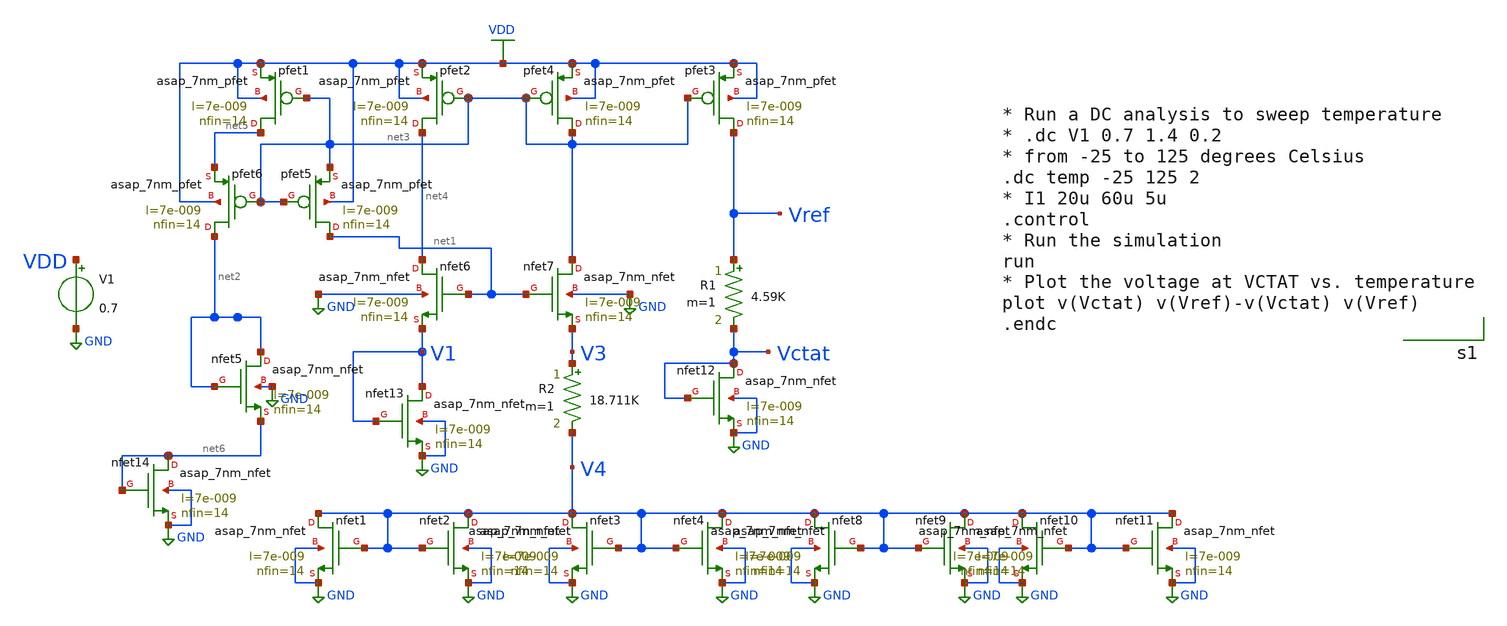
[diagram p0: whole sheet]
** sch_path: xschem/Circuits/BGR_Current_mirror.sch
* AsahiroKenpachi/asap_7nm_Xschem/asap_7nm_nfet.sym:
* Copyright 2021 Stefan Frederik Schippers
* Licensed under the Apache License, Version 2.0 (the "License");
**.subckt BGR_Current_mirror
Xnfet5 net2 net2 net6 GND asap_7nm_nfet l=7e-009 nfin=14
Xpfet1 net5 net3 VDD VDD asap_7nm_pfet l=7e-009 nfin=14
Xpfet2 net4 net3 VDD VDD asap_7nm_pfet l=7e-009 nfin=14
Xpfet3 Vref net3 VDD VDD asap_7nm_pfet l=7e-009 nfin=14
Xpfet4 net3 net3 VDD VDD asap_7nm_pfet l=7e-009 nfin=14
Xpfet5 net1 net3 net3 VDD asap_7nm_pfet l=7e-009 nfin=14
Xnfet1 V4 V4 GND GND asap_7nm_nfet l=7e-009 nfin=14
Xnfet2 V4 V4 GND GND asap_7nm_nfet l=7e-009 nfin=14
Xnfet3 V4 V4 GND GND asap_7nm_nfet l=7e-009 nfin=14
Xnfet4 V4 V4 GND GND asap_7nm_nfet l=7e-009 nfin=14
Xnfet8 V4 V4 GND GND asap_7nm_nfet l=7e-009 nfin=14
Xnfet9 V4 V4 GND GND asap_7nm_nfet l=7e-009 nfin=14
Xnfet10 V4 V4 GND GND asap_7nm_nfet l=7e-009 nfin=14
Xnfet11 V4 V4 GND GND asap_7nm_nfet l=7e-009 nfin=14
Xnfet12 Vctat Vctat GND GND asap_7nm_nfet l=7e-009 nfin=14
V1 VDD GND 0.7
Xnfet13 V1 V1 GND GND asap_7nm_nfet l=7e-009 nfin=14
Xpfet6 net2 net3 net5 VDD asap_7nm_pfet l=7e-009 nfin=14
Xnfet14 net6 net6 GND GND asap_7nm_nfet l=7e-009 nfin=14
R2 V3 V4 18.711K m=1
R1 Vref Vctat 4.59K m=1
Xnfet6 net4 net1 V1 GND asap_7nm_nfet l=7e-009 nfin=14
Xnfet7 net3 net1 V3 GND asap_7nm_nfet l=7e-009 nfin=14
**** begin user architecture code


* Run a DC analysis to sweep temperature
* .dc V1 0.7 1.4 0.2
* from -25 to 125 degrees Celsius
.dc temp -25 125 2
* I1 20u 60u 5u
.control
* Run the simulation
run
* Plot the voltage at VCTAT vs. temperature
plot v(Vctat) v(Vref)-v(Vctat) v(Vref)
.endc


**** end user architecture code
**.ends
.GLOBAL GND
.GLOBAL VDD
**** begin user architecture code

.subckt asap_7nm_nfet S G D B l=@l nfin=@nfin
	nnmos_finfet S G D B BSIMCMG_osdi_N l=@l nfin=@nfin
.ends asap_7nm_nfet

.model BSIMCMG_osdi_N BSIMCMG_va (  TYPE = 1
************************************************************
*                         general                          *
************************************************************ version = 107             bulkmod = 1
*+               igcmod  = 1               igbmod  = 0              gidlmod = 1               iimod   = 0
*+               geomod  = 1               rdsmod  = 0              rgatemod= 0               rgeomod = 0
*+               shmod   = 0               nqsmod  = 0              coremod = 0               cgeomod = 0
*+               capmod  = 0               tnom    = 25             eot     = 1e-009          eotbox  = 1.4e-007
*+        eotacc  = 1e-010          tfin    = 6.5e-009       toxp    = 2.1e-009        nbody   = 1e+022
*+          phig    = 4.2466          epsrox  = 3.9            epsrsub = 11.9            easub   = 4.05
*+            ni0sub  = 1.1e+016        bg0sub  = 1.17           nc0sub  = 2.86e+025       nsd     = 2e+026
*+          ngate   = 0               nseg    = 5              l       = 2.1e-008        xl      = 1e-009
*+          lint    = -2e-009         dlc     = 0              dlbin   = 0               hfin    = 3.2e-008
*+        deltaw  = 0               deltawcv= 0              sdterm  = 0               epsrsp  = 3.9
*+             nfin    = 1 toxg    = 1.80e-009
************************************************************
*                            dc                            *
************************************************************ cit     = 0               cdsc    =
*+ 0.01            cdscd   = 0.01            dvt0    = 0.05           dvt1    = 0.47            phin    =
*+ 0.05            eta0    = 0.07            dsub    = 0.35           k1rsce  = 0               lpe0    = 0
*+               dvtshift= 0               qmfactor= 2.5            etaqm   = 0.54            qm0     = 0.001           pqm
*+     = 0.66            u0      = 0.0303         etamob  = 2               up      = 0               ua
*+      = 0.55            eu      = 1.2            ud      = 0               ucs     = 1
*+               rdswmin = 0               rdsw    = 200            wr      = 1               rswmin  = 0
*+               rdwmin  = 0               rshs    = 0              rshd    = 0               vsat    = 70000
*+           deltavsat= 0.2             ksativ  = 2              mexp    = 4               ptwg    = 30              pclm
*+    = 0.05            pclmg   = 0              pdibl1  = 0               pdibl2  = 0.002           drout
*+   = 1               pvag    = 0              fpitch  = 2.7e-008        rth0    = 0.225           cth0
*+    = 1.243e-006      wth0    = 2.6e-007       lcdscd  = 5e-005          lcdscdr = 5e-005          lrdsw
*+   = 0.2             lvsat   = 0
************************************************************
*                         leakage                          *
************************************************************ aigc    = 0.014           bigc    =
*+ 0.005           cigc    = 0.25            dlcigs  = 1e-009         dlcigd  = 1e-009          aigs    =
*+ 0.0115          aigd    = 0.0115          bigs    = 0.00332        bigd    = 0.00332         cigs    =
*+ 0.35            cigd    = 0.35            poxedge = 1.1            agidl   = 1e-012          agisl   =
*+ 1e-012          bgidl   = 10000000        bgisl   = 10000000       egidl   = 0.35            egisl   =
*+ 0.35
************************************************************
*                            rf                            *
************************************************************
************************************************************
*                         junction                         *
************************************************************
************************************************************
*                       capacitance                        *
************************************************************ cfs     = 0               cfd     = 0
*+               cgso    = 1.6e-010        cgdo    = 1.6e-010       cgsl    = 0               cgdl    = 0
*+               ckappas = 0.6             ckappad = 0.6            cgbo    = 0               cgbl    = 0
************************************************************
*                       temperature                        *
************************************************************ tbgasub = 0.000473        tbgbsub = 636
*+             kt1     = 0               kt1l    = 0              ute     = -0.7            utl     = 0
*+               ua1     = 0.001032        ud1     = 0              ucste   = -0.004775       at      = 0.001
*+           ptwgt   = 0.004           tmexp   = 0              prt     = 0               tgidl   = -0.007
*+          igt     = 2.5
************************************************************
*                          noise                           *
************************************************************
**)
.control
pre_osdi /home/hprcse/Documents/test/bsimcmg.osdi
.endc



.subckt asap_7nm_pfet S G D B l=@l nfin=@nfin
	npmos_finfet S G D B BSIMCMG_osdi_P l=@l nfin=@nfin
.ends asap_7nm_pfet

.model BSIMCMG_osdi_P BSIMCMG_va (  TYPE = 0

************************************************************
*                         general                          *
************************************************************ version = 107             bulkmod = 1
*+               igcmod  = 1               igbmod  = 0              gidlmod = 1               iimod   = 0
*+               geomod  = 1               rdsmod  = 0              rgatemod= 0               rgeomod = 0
*+               shmod   = 0               nqsmod  = 0              coremod = 0               cgeomod = 0
*+               capmod  = 0               tnom    = 25             eot     = 1e-009          eotbox  = 1.4e-007
*+        eotacc  = 3e-010          tfin    = 6.5e-009       toxp    = 2.1e-009        nbody   = 1e+022
*+          phig    = 4.9278          epsrox  = 3.9            epsrsub = 11.9            easub   = 4.05
*+            ni0sub  = 1.1e+016        bg0sub  = 1.17           nc0sub  = 2.86e+025       nsd     = 2e+026
*+          ngate   = 0               nseg    = 5              l       = 2.1e-008        xl      = 1e-009
*+          lint    = -2.5e-009       dlc     = 0              dlbin   = 0               hfin    = 3.2e-008
*+        deltaw  = 0               deltawcv= 0              sdterm  = 0               epsrsp  = 3.9
*+             nfin    = 1 toxg    = 1.8e-009
************************************************************
*                            dc                            *
************************************************************ cit     = 0               cdsc    =
*+ 0.003469        cdscd   = 0.001486        dvt0    = 0.05           dvt1    = 0.36            phin    = 0.05
*+            eta0    = 0.094           dsub    = 0.24           k1rsce  = 0               lpe0    = 0
*+               dvtshift= 0               qmfactor= 0              etaqm   = 0.54            qm0     = 2.183e-012      pqm
*+     = 0.66            u0      = 0.0237         etamob  = 4               up      = 0               ua
*+      = 1.133           eu      = 0.05           ud      = 0.0105          ucs     = 0.2672
*+          rdswmin = 0               rdsw    = 200            wr      = 1               rswmin  = 0
*+               rdwmin  = 0               rshs    = 0              rshd    = 0               vsat    = 60000
*+           deltavsat= 0.17            ksativ  = 1.592          mexp    = 2.491           ptwg    = 25              pclm
*+    = 0.01            pclmg   = 1              pdibl1  = 800             pdibl2  = 0.005704        drout
*+   = 4.97            pvag    = 200            fpitch  = 2.7e-008        rth0    = 0.15            cth0
*+    = 1.243e-006      wth0    = 2.6e-007       lcdscd  = 0               lcdscdr = 0               lrdsw
*+   = 1.3             lvsat   = 1441
************************************************************
*                         leakage                          *
************************************************************ aigc    = 0.007           bigc    =
*+ 0.0015          cigc    = 1               dlcigs  = 5e-009         dlcigd  = 5e-009          aigs    =
*+ 0.006           aigd    = 0.006           bigs    = 0.001944       bigd    = 0.001944        cigs    = 1
*+               cigd    = 1               poxedge = 1.152          agidl   = 2e-012          agisl   = 2e-012
*+          bgidl   = 1.5e+008        bgisl   = 1.5e+008       egidl   = 1.142           egisl   = 1.142
************************************************************
*                            rf                            *
************************************************************
************************************************************
*                         junction                         *
************************************************************
************************************************************
*                       capacitance                        *
************************************************************ cfs     = 0               cfd     = 0
*+               cgso    = 1.6e-010        cgdo    = 1.6e-010       cgsl    = 0               cgdl    = 0
*+               ckappas = 0.6             ckappad = 0.6            cgbo    = 0               cgbl    = 0
************************************************************
*                       temperature                        *
************************************************************ tbgasub = 0.000473        tbgbsub = 636
*+             kt1     = 0               kt1l    = 0              ute     = -1.2            utl     = 0
*+               ua1     = 0.001032        ud1     = 0              ucste   = -0.004775       at      = 0.001
*+           ptwgt   = 0.004           tmexp   = 0              prt     = 0               tgidl   = -0.007
*+          igt     = 2.5
************************************************************
*                          noise                           *
************************************************************
**)
.control
pre_osdi /home/hprcse/Documents/test/bsimcmg.osdi
.endc


**** end user architecture code
.end
